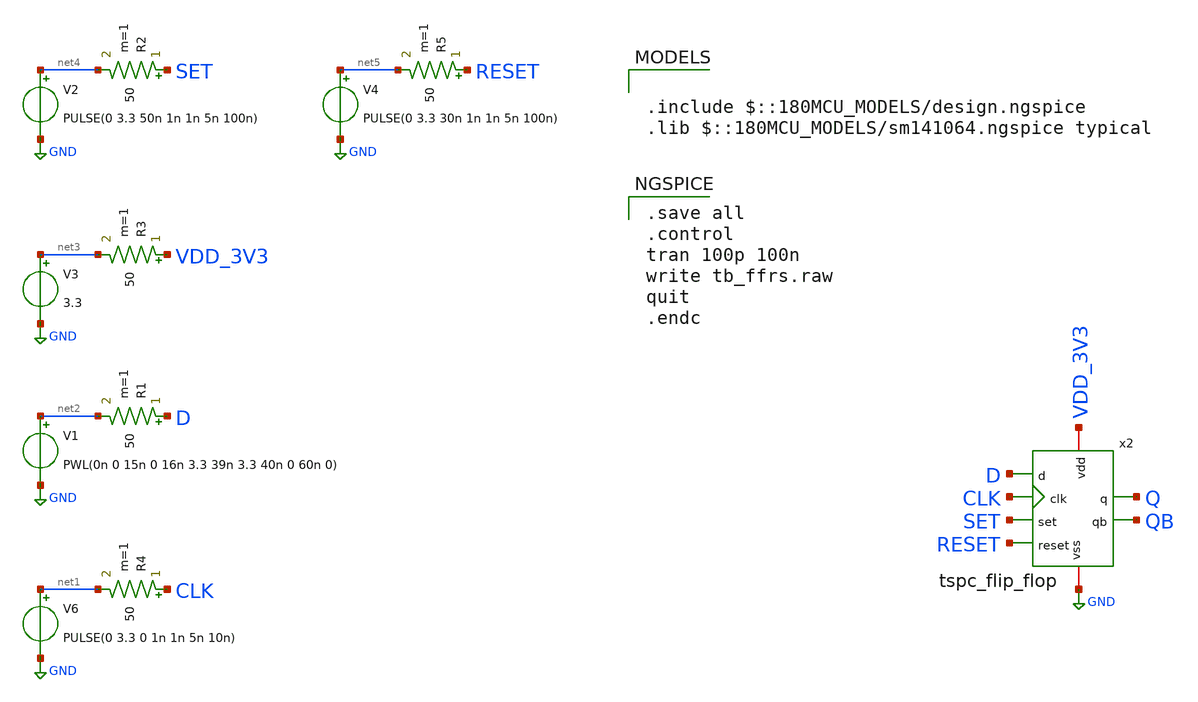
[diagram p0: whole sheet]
** sch_path: designs/libs/tspc_flip_flop/tspc_flip_flop_tb.sch
**.subckt tspc_flip_flop_tb
V6 net1 GND PULSE(0 3.3 0 1n 1n 5n 10n)
R4 CLK net1 50 m=1
V1 net2 GND PWL(0n 0 15n 0 16n 3.3 39n 3.3 40n 0 60n 0)
R1 D net2 50 m=1
V3 net3 GND 3.3
R3 VDD_3V3 net3 50 m=1
V2 net4 GND PULSE(0 3.3 50n 1n 1n 5n 100n)
R2 SET net4 50 m=1
V4 net5 GND PULSE(0 3.3 30n 1n 1n 5n 100n)
R5 RESET net5 50 m=1
x2 VDD_3V3 GND D CLK SET RESET Q QB tspc_flip_flop
**** begin user architecture code

.include $::180MCU_MODELS/design.ngspice
.lib $::180MCU_MODELS/sm141064.ngspice typical


.save all
.control
tran 100p 100n
write tb_ffrs.raw
quit
.endc

**** end user architecture code
**.ends

* expanding   symbol:  libs/tspc_flip_flop/tspc_flip_flop.sym # of pins=8
** sym_path: designs/libs/tspc_flip_flop/tspc_flip_flop.sym
** sch_path: designs/libs/tspc_flip_flop/tspc_flip_flop.sch
.subckt tspc_flip_flop vdd vss d clk set reset q qb
*.iopin vdd
*.iopin vss
*.ipin d
*.ipin clk
*.ipin set
*.ipin reset
*.opin q
*.opin qb
XM1 b1 d vss vss nfet_03v3 L=0.28u W=1u nf=1 ad='int((nf+1)/2) * W/nf * 0.18u' as='int((nf+2)/2) * W/nf * 0.18u'
+ pd='2*int((nf+1)/2) * (W/nf + 0.18u)' ps='2*int((nf+2)/2) * (W/nf + 0.18u)' nrd='0.18u / W' nrs='0.18u / W'
+ sa=0 sb=0 sd=0 m=1
XM2 b1 clk net1 net1 pfet_03v3 L=0.28u W=2u nf=1 ad='int((nf+1)/2) * W/nf * 0.18u' as='int((nf+2)/2) * W/nf * 0.18u'
+ pd='2*int((nf+1)/2) * (W/nf + 0.18u)' ps='2*int((nf+2)/2) * (W/nf + 0.18u)' nrd='0.18u / W' nrs='0.18u / W'
+ sa=0 sb=0 sd=0 m=1
XM3 net1 d vdd vdd pfet_03v3 L=0.28u W=2u nf=1 ad='int((nf+1)/2) * W/nf * 0.18u' as='int((nf+2)/2) * W/nf * 0.18u'
+ pd='2*int((nf+1)/2) * (W/nf + 0.18u)' ps='2*int((nf+2)/2) * (W/nf + 0.18u)' nrd='0.18u / W' nrs='0.18u / W'
+ sa=0 sb=0 sd=0 m=1
XM4 b2 clk vdd vdd pfet_03v3 L=0.28u W=2u nf=1 ad='int((nf+1)/2) * W/nf * 0.18u' as='int((nf+2)/2) * W/nf * 0.18u'
+ pd='2*int((nf+1)/2) * (W/nf + 0.18u)' ps='2*int((nf+2)/2) * (W/nf + 0.18u)' nrd='0.18u / W' nrs='0.18u / W'
+ sa=0 sb=0 sd=0 m=1
XM5 b2 b1 net2 vss nfet_03v3 L=0.28u W=1u nf=1 ad='int((nf+1)/2) * W/nf * 0.18u' as='int((nf+2)/2) * W/nf * 0.18u'
+ pd='2*int((nf+1)/2) * (W/nf + 0.18u)' ps='2*int((nf+2)/2) * (W/nf + 0.18u)' nrd='0.18u / W' nrs='0.18u / W'
+ sa=0 sb=0 sd=0 m=1
XM6 net2 clk vss vss nfet_03v3 L=0.28u W=1u nf=1 ad='int((nf+1)/2) * W/nf * 0.18u' as='int((nf+2)/2) * W/nf * 0.18u'
+ pd='2*int((nf+1)/2) * (W/nf + 0.18u)' ps='2*int((nf+2)/2) * (W/nf + 0.18u)' nrd='0.18u / W' nrs='0.18u / W'
+ sa=0 sb=0 sd=0 m=1
XM7 net4 b2 vss vss nfet_03v3 L=0.28u W=1u nf=1 ad='int((nf+1)/2) * W/nf * 0.18u' as='int((nf+2)/2) * W/nf * 0.18u'
+ pd='2*int((nf+1)/2) * (W/nf + 0.18u)' ps='2*int((nf+2)/2) * (W/nf + 0.18u)' nrd='0.18u / W' nrs='0.18u / W'
+ sa=0 sb=0 sd=0 m=1
XM8 b3 clk net4 vss nfet_03v3 L=0.28u W=1u nf=1 ad='int((nf+1)/2) * W/nf * 0.18u' as='int((nf+2)/2) * W/nf * 0.18u'
+ pd='2*int((nf+1)/2) * (W/nf + 0.18u)' ps='2*int((nf+2)/2) * (W/nf + 0.18u)' nrd='0.18u / W' nrs='0.18u / W'
+ sa=0 sb=0 sd=0 m=1
XM9 b3 set net3 net3 pfet_03v3 L=0.28u W=2u nf=1 ad='int((nf+1)/2) * W/nf * 0.18u' as='int((nf+2)/2) * W/nf * 0.18u'
+ pd='2*int((nf+1)/2) * (W/nf + 0.18u)' ps='2*int((nf+2)/2) * (W/nf + 0.18u)' nrd='0.18u / W' nrs='0.18u / W'
+ sa=0 sb=0 sd=0 m=1
XM10 net3 b2 vdd vdd pfet_03v3 L=0.28u W=2u nf=1 ad='int((nf+1)/2) * W/nf * 0.18u' as='int((nf+2)/2) * W/nf * 0.18u'
+ pd='2*int((nf+1)/2) * (W/nf + 0.18u)' ps='2*int((nf+2)/2) * (W/nf + 0.18u)' nrd='0.18u / W' nrs='0.18u / W'
+ sa=0 sb=0 sd=0 m=1
XM11 b3 net5 vdd vdd pfet_03v3 L=0.28u W=2u nf=1 ad='int((nf+1)/2) * W/nf * 0.18u' as='int((nf+2)/2) * W/nf * 0.18u'
+ pd='2*int((nf+1)/2) * (W/nf + 0.18u)' ps='2*int((nf+2)/2) * (W/nf + 0.18u)' nrd='0.18u / W' nrs='0.18u / W'
+ sa=0 sb=0 sd=0 m=1
XM12 b3 set vss vss nfet_03v3 L=0.28u W=1u nf=1 ad='int((nf+1)/2) * W/nf * 0.18u' as='int((nf+2)/2) * W/nf * 0.18u'
+ pd='2*int((nf+1)/2) * (W/nf + 0.18u)' ps='2*int((nf+2)/2) * (W/nf + 0.18u)' nrd='0.18u / W' nrs='0.18u / W'
+ sa=0 sb=0 sd=0 m=1
XM13 q b3 vdd vdd pfet_03v3 L=0.28u W=2u nf=1 ad='int((nf+1)/2) * W/nf * 0.18u' as='int((nf+2)/2) * W/nf * 0.18u'
+ pd='2*int((nf+1)/2) * (W/nf + 0.18u)' ps='2*int((nf+2)/2) * (W/nf + 0.18u)' nrd='0.18u / W' nrs='0.18u / W'
+ sa=0 sb=0 sd=0 m=1
XM14 q b3 vss vss nfet_03v3 L=0.28u W=1u nf=1 ad='int((nf+1)/2) * W/nf * 0.18u' as='int((nf+2)/2) * W/nf * 0.18u'
+ pd='2*int((nf+1)/2) * (W/nf + 0.18u)' ps='2*int((nf+2)/2) * (W/nf + 0.18u)' nrd='0.18u / W' nrs='0.18u / W'
+ sa=0 sb=0 sd=0 m=1
XM15 net5 reset vdd vdd pfet_03v3 L=0.28u W=2u nf=1 ad='int((nf+1)/2) * W/nf * 0.18u' as='int((nf+2)/2) * W/nf * 0.18u'
+ pd='2*int((nf+1)/2) * (W/nf + 0.18u)' ps='2*int((nf+2)/2) * (W/nf + 0.18u)' nrd='0.18u / W' nrs='0.18u / W'
+ sa=0 sb=0 sd=0 m=1
XM16 net5 reset vss vss nfet_03v3 L=0.28u W=1u nf=1 ad='int((nf+1)/2) * W/nf * 0.18u' as='int((nf+2)/2) * W/nf * 0.18u'
+ pd='2*int((nf+1)/2) * (W/nf + 0.18u)' ps='2*int((nf+2)/2) * (W/nf + 0.18u)' nrd='0.18u / W' nrs='0.18u / W'
+ sa=0 sb=0 sd=0 m=1
XM17 qb q vdd vdd pfet_03v3 L=0.28u W=2u nf=1 ad='int((nf+1)/2) * W/nf * 0.18u' as='int((nf+2)/2) * W/nf * 0.18u'
+ pd='2*int((nf+1)/2) * (W/nf + 0.18u)' ps='2*int((nf+2)/2) * (W/nf + 0.18u)' nrd='0.18u / W' nrs='0.18u / W'
+ sa=0 sb=0 sd=0 m=1
XM18 qb q vss vss nfet_03v3 L=0.28u W=1u nf=1 ad='int((nf+1)/2) * W/nf * 0.18u' as='int((nf+2)/2) * W/nf * 0.18u'
+ pd='2*int((nf+1)/2) * (W/nf + 0.18u)' ps='2*int((nf+2)/2) * (W/nf + 0.18u)' nrd='0.18u / W' nrs='0.18u / W'
+ sa=0 sb=0 sd=0 m=1
.ends

.GLOBAL GND
.end
